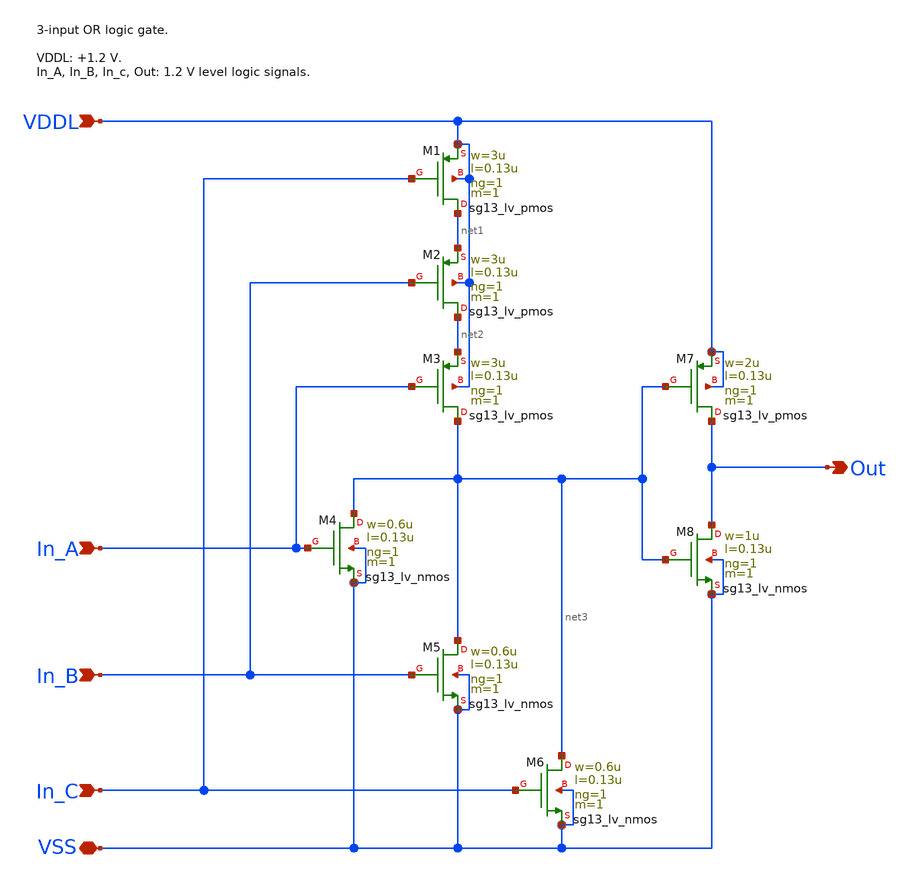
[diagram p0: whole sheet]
** sch_path: sar_adc/xschem/blocks/logic_elements/3-input_OR/3-input_OR.sch
**.subckt 3-input_OR Out VSS VDDL In_A In_B In_C
*.opin Out
*.iopin VSS
*.ipin VDDL
*.ipin In_A
*.ipin In_B
*.ipin In_C
XM2 net2 In_B net1 VDDL sg13_lv_pmos w=3u l=0.13u ng=1 m=1 mm_ok=1
XM3 net3 In_A net2 VDDL sg13_lv_pmos w=3u l=0.13u ng=1 m=1 mm_ok=1
XM4 net3 In_A VSS VSS sg13_lv_nmos w=0.6u l=0.13u ng=1 m=1 mm_ok=1
XM5 net3 In_B VSS VSS sg13_lv_nmos w=0.6u l=0.13u ng=1 m=1 mm_ok=1
XM7 Out net3 VDDL VDDL sg13_lv_pmos w=2u l=0.13u ng=1 m=1 mm_ok=1
XM8 Out net3 VSS VSS sg13_lv_nmos w=1u l=0.13u ng=1 m=1 mm_ok=1
XM6 net3 In_C VSS VSS sg13_lv_nmos w=0.6u l=0.13u ng=1 m=1 mm_ok=1
XM1 net1 In_C VDDL VDDL sg13_lv_pmos w=3u l=0.13u ng=1 m=1 mm_ok=1
**.ends
.end
